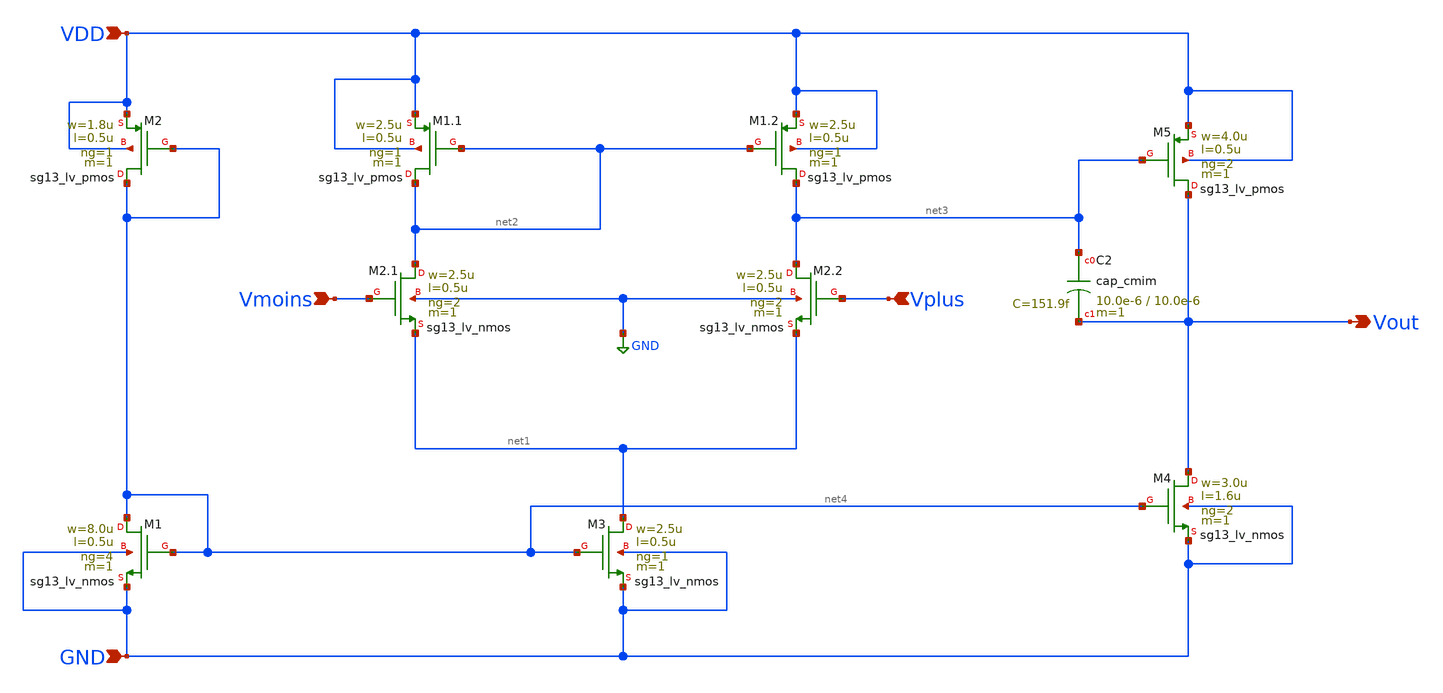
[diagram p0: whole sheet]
** sch_path: OTA.sch
**.subckt OTA Vmoins Vplus VDD GND Vout
*.ipin Vmoins
*.ipin Vplus
*.ipin VDD
*.ipin GND
*.opin Vout
XM3 net1 net4 GND GND sg13_lv_nmos w=2.5u l=0.5u ng=1 m=1 mm_ok=1
XM2.1 net2 Vmoins net1 GND sg13_lv_nmos w=2.5u l=0.5u ng=2 m=1 mm_ok=1
XM2.2 net3 Vplus net1 GND sg13_lv_nmos w=2.5u l=0.5u ng=2 m=1 mm_ok=1
XM1.1 net2 net2 VDD VDD sg13_lv_pmos w=2.5u l=0.5u ng=1 m=1 mm_ok=1
XM1.2 net3 net2 VDD VDD sg13_lv_pmos w=2.5u l=0.5u ng=1 m=1 mm_ok=1
XM4 Vout net4 GND GND sg13_lv_nmos w=3.0u l=1.6u ng=2 m=1 mm_ok=1
XM5 Vout net3 VDD VDD sg13_lv_pmos w=4.0u l=0.5u ng=2 m=1 mm_ok=1
XC2 net3 Vout cap_cmim w=10.0e-6 l=10.0e-6 m=1 mm_ok=1
XM1 net4 net4 GND GND sg13_lv_nmos w=8.0u l=0.5u ng=4 m=1 mm_ok=1
XM2 net4 net4 VDD VDD sg13_lv_pmos w=1.8u l=0.5u ng=1 m=1 mm_ok=1
**.ends
.GLOBAL GND
.end
